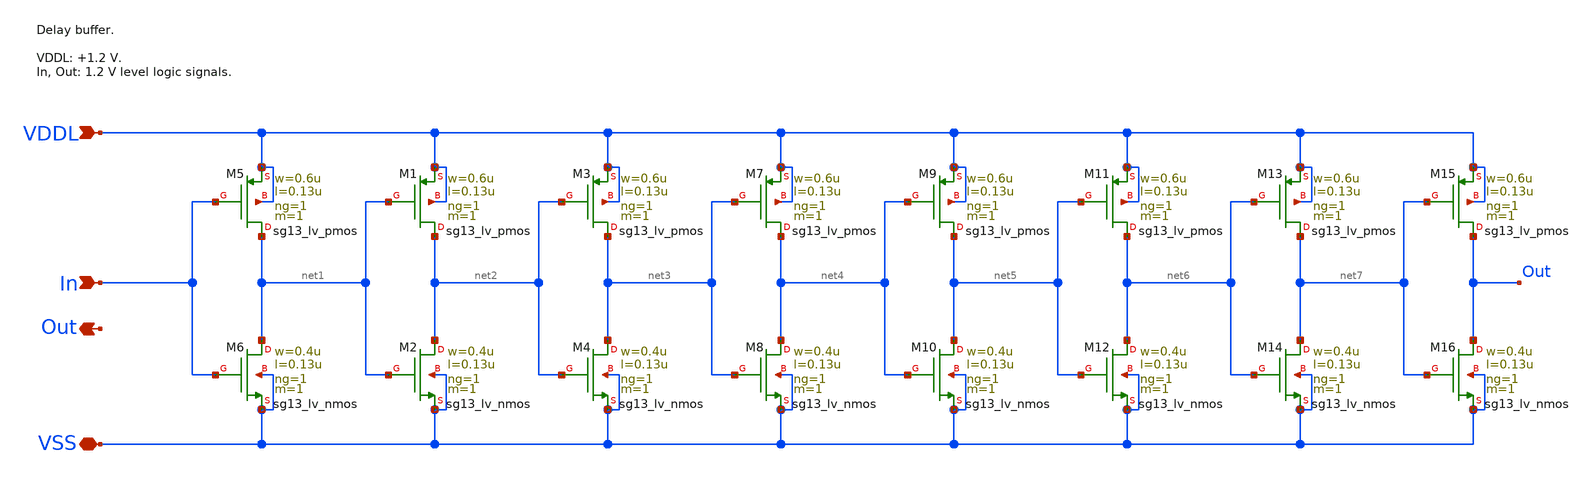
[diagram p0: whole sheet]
** sch_path: sar_adc/xschem/blocks/delay_buffer/delay_buffer.sch
**.subckt delay_buffer VSS In VDDL Out
*.iopin VSS
*.ipin In
*.ipin VDDL
*.opin Out
XM5 net1 In VDDL VDDL sg13_lv_pmos w=0.6u l=0.13u ng=1 m=1 mm_ok=1
XM6 net1 In VSS VSS sg13_lv_nmos w=0.4u l=0.13u ng=1 m=1 mm_ok=1
XM1 net2 net1 VDDL VDDL sg13_lv_pmos w=0.6u l=0.13u ng=1 m=1 mm_ok=1
XM2 net2 net1 VSS VSS sg13_lv_nmos w=0.4u l=0.13u ng=1 m=1 mm_ok=1
XM3 net3 net2 VDDL VDDL sg13_lv_pmos w=0.6u l=0.13u ng=1 m=1 mm_ok=1
XM4 net3 net2 VSS VSS sg13_lv_nmos w=0.4u l=0.13u ng=1 m=1 mm_ok=1
XM7 net4 net3 VDDL VDDL sg13_lv_pmos w=0.6u l=0.13u ng=1 m=1 mm_ok=1
XM8 net4 net3 VSS VSS sg13_lv_nmos w=0.4u l=0.13u ng=1 m=1 mm_ok=1
XM9 net5 net4 VDDL VDDL sg13_lv_pmos w=0.6u l=0.13u ng=1 m=1 mm_ok=1
XM10 net5 net4 VSS VSS sg13_lv_nmos w=0.4u l=0.13u ng=1 m=1 mm_ok=1
XM11 net6 net5 VDDL VDDL sg13_lv_pmos w=0.6u l=0.13u ng=1 m=1 mm_ok=1
XM12 net6 net5 VSS VSS sg13_lv_nmos w=0.4u l=0.13u ng=1 m=1 mm_ok=1
XM13 net7 net6 VDDL VDDL sg13_lv_pmos w=0.6u l=0.13u ng=1 m=1 mm_ok=1
XM14 net7 net6 VSS VSS sg13_lv_nmos w=0.4u l=0.13u ng=1 m=1 mm_ok=1
XM15 Out net7 VDDL VDDL sg13_lv_pmos w=0.6u l=0.13u ng=1 m=1 mm_ok=1
XM16 Out net7 VSS VSS sg13_lv_nmos w=0.4u l=0.13u ng=1 m=1 mm_ok=1
**.ends
.end
